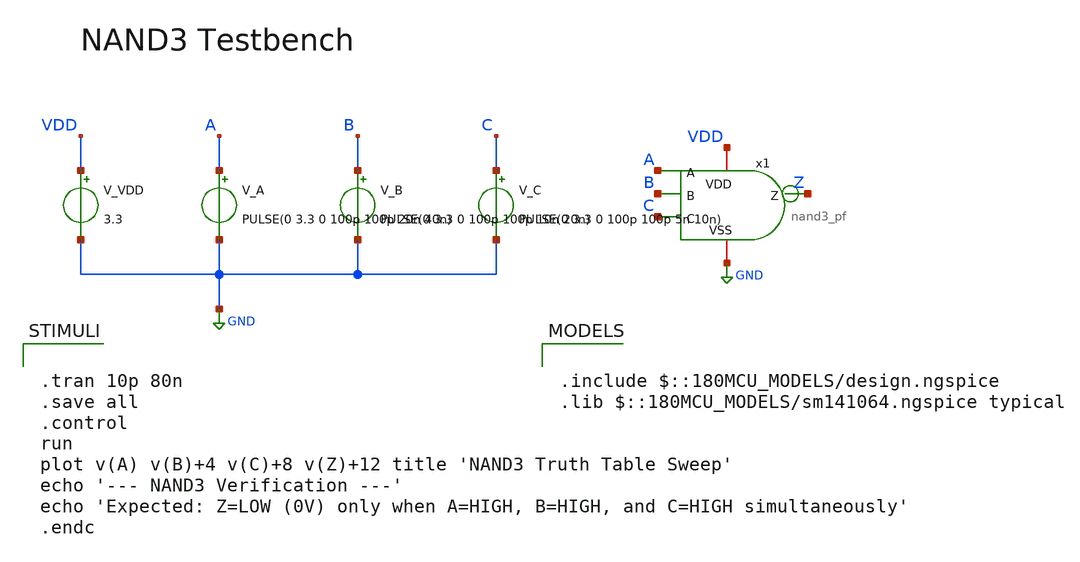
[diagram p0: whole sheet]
** sch_path: designs/libs/core_analog/pfd/nand3_tb.sch
**.subckt nand3_tb
V_VDD VDD GND 3.3
V_A A GND PULSE(0 3.3 0 100p 100p 20n 40n)
V_B B GND PULSE(0 3.3 0 100p 100p 10n 20n)
V_C C GND PULSE(0 3.3 0 100p 100p 5n 10n)
x1 VDD Z A B C GND nand3_pf
**** begin user architecture code


.tran 10p 80n
.save all
.control
run
plot v(A) v(B)+4 v(C)+8 v(Z)+12 title 'NAND3 Truth Table Sweep'
echo '--- NAND3 Verification ---'
echo 'Expected: Z=LOW (0V) only when A=HIGH, B=HIGH, and C=HIGH simultaneously'
.endc



.include $::180MCU_MODELS/design.ngspice
.lib $::180MCU_MODELS/sm141064.ngspice typical

**** end user architecture code
**.ends

* expanding   symbol:  libs/core_analog/pfd/nand3_pf.sym # of pins=6
** sym_path: designs/libs/core_analog/pfd/nand3_pf.sym
** sch_path: designs/libs/core_analog/pfd/nand3_pf.sch
.subckt nand3_pf VDD Z A B C VSS
*.iopin VDD
*.iopin VSS
*.ipin A
*.ipin B
*.ipin C
*.opin Z
XMp1 Z A VDD VDD pfet_03v3 L=0.28u W=1u nf=1 ad='int((nf+1)/2) * W/nf * 0.18u' as='int((nf+2)/2) * W/nf * 0.18u'
+ pd='2*int((nf+1)/2) * (W/nf + 0.18u)' ps='2*int((nf+2)/2) * (W/nf + 0.18u)' nrd='0.18u / W' nrs='0.18u / W'
+ sa=0 sb=0 sd=0 m=1
XMp2 Z B VDD VDD pfet_03v3 L=0.28u W=1u nf=1 ad='int((nf+1)/2) * W/nf * 0.18u' as='int((nf+2)/2) * W/nf * 0.18u'
+ pd='2*int((nf+1)/2) * (W/nf + 0.18u)' ps='2*int((nf+2)/2) * (W/nf + 0.18u)' nrd='0.18u / W' nrs='0.18u / W'
+ sa=0 sb=0 sd=0 m=1
XMp3 Z C VDD VDD pfet_03v3 L=0.28u W=1u nf=1 ad='int((nf+1)/2) * W/nf * 0.18u' as='int((nf+2)/2) * W/nf * 0.18u'
+ pd='2*int((nf+1)/2) * (W/nf + 0.18u)' ps='2*int((nf+2)/2) * (W/nf + 0.18u)' nrd='0.18u / W' nrs='0.18u / W'
+ sa=0 sb=0 sd=0 m=1
XMn1 Z A net1 VSS nfet_03v3 L=0.28u W=1.5u nf=1 ad='int((nf+1)/2) * W/nf * 0.18u' as='int((nf+2)/2) * W/nf * 0.18u'
+ pd='2*int((nf+1)/2) * (W/nf + 0.18u)' ps='2*int((nf+2)/2) * (W/nf + 0.18u)' nrd='0.18u / W' nrs='0.18u / W'
+ sa=0 sb=0 sd=0 m=1
XMn2 net1 B net2 VSS nfet_03v3 L=0.28u W=1.5u nf=1 ad='int((nf+1)/2) * W/nf * 0.18u' as='int((nf+2)/2) * W/nf * 0.18u'
+ pd='2*int((nf+1)/2) * (W/nf + 0.18u)' ps='2*int((nf+2)/2) * (W/nf + 0.18u)' nrd='0.18u / W' nrs='0.18u / W'
+ sa=0 sb=0 sd=0 m=1
XMn3 net2 C VSS VSS nfet_03v3 L=0.28u W=1.5u nf=1 ad='int((nf+1)/2) * W/nf * 0.18u' as='int((nf+2)/2) * W/nf * 0.18u'
+ pd='2*int((nf+1)/2) * (W/nf + 0.18u)' ps='2*int((nf+2)/2) * (W/nf + 0.18u)' nrd='0.18u / W' nrs='0.18u / W'
+ sa=0 sb=0 sd=0 m=1
.ends

.GLOBAL GND
.end
